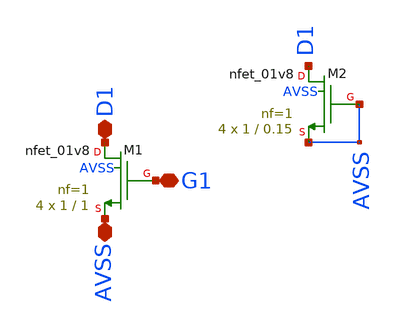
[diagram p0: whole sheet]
** sch_path: magic/nmos_startup.sch
**.subckt nmos_startup AVSS D1 G1
*.iopin AVSS
*.iopin D1
*.iopin G1
XM1 D1 G1 AVSS AVSS sky130_fd_pr__nfet_01v8 L=1 W=1 nf=1 ad='int((nf+1)/2) * W/nf * 0.29' as='int((nf+2)/2) * W/nf * 0.29'
+ pd='2*int((nf+1)/2) * (W/nf + 0.29)' ps='2*int((nf+2)/2) * (W/nf + 0.29)' nrd='0.29 / W' nrs='0.29 / W'
+ sa=0 sb=0 sd=0 mult=4 m=4
XM2 D1 AVSS AVSS AVSS sky130_fd_pr__nfet_01v8 L=0.15 W=1 nf=1 ad='int((nf+1)/2) * W/nf * 0.29' as='int((nf+2)/2) * W/nf * 0.29'
+ pd='2*int((nf+1)/2) * (W/nf + 0.29)' ps='2*int((nf+2)/2) * (W/nf + 0.29)' nrd='0.29 / W' nrs='0.29 / W'
+ sa=0 sb=0 sd=0 mult=4 m=4
**.ends
.end
